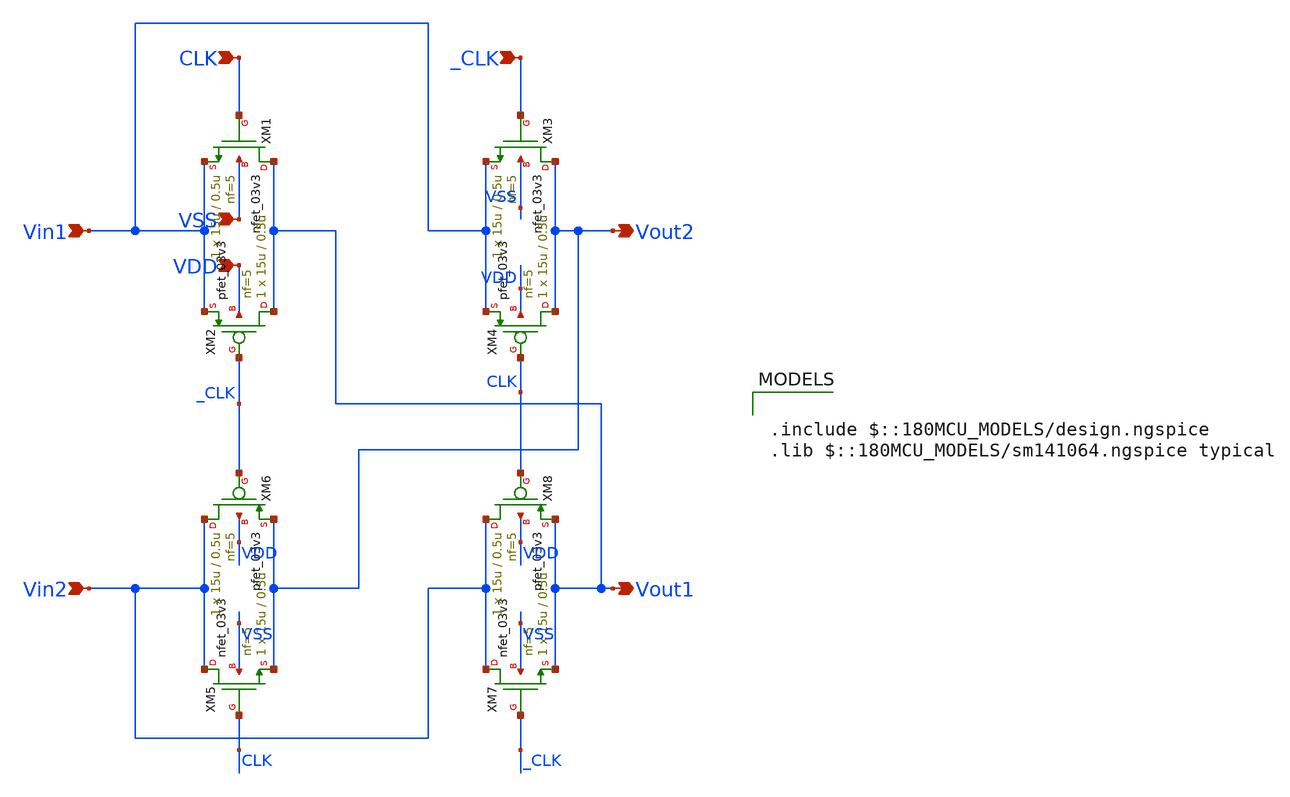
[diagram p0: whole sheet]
** sch_path: ISSCC26/submitted_notebooks/Low Mismatch 4 Channels Instrumentation Amplifier EEG/Chopper Switch/Schmatic and Testbench/switch_A.sch
**.subckt switch_A Vin1 Vout2 Vin2 Vout1 CLK _CLK VDD VSS
*.ipin Vin1
*.opin Vout2
*.ipin Vin2
*.opin Vout1
*.ipin CLK
*.ipin _CLK
*.ipin VDD
*.ipin VSS
XM1 Vout1 CLK Vin1 VSS nfet_03v3 L=0.5u W=15u nf=5 ad='int((nf+1)/2) * W/nf * 0.18u' as='int((nf+2)/2) * W/nf * 0.18u'
+ pd='2*int((nf+1)/2) * (W/nf + 0.18u)' ps='2*int((nf+2)/2) * (W/nf + 0.18u)' nrd='0.18u / W' nrs='0.18u / W'
+ sa=0 sb=0 sd=0 m=1
XM2 Vout1 _CLK Vin1 VDD pfet_03v3 L=0.5u W=15u nf=5 ad='int((nf+1)/2) * W/nf * 0.18u' as='int((nf+2)/2) * W/nf * 0.18u'
+ pd='2*int((nf+1)/2) * (W/nf + 0.18u)' ps='2*int((nf+2)/2) * (W/nf + 0.18u)' nrd='0.18u / W' nrs='0.18u / W'
+ sa=0 sb=0 sd=0 m=1
XM3 Vout2 _CLK Vin1 VSS nfet_03v3 L=0.5u W=15u nf=5 ad='int((nf+1)/2) * W/nf * 0.18u' as='int((nf+2)/2) * W/nf * 0.18u'
+ pd='2*int((nf+1)/2) * (W/nf + 0.18u)' ps='2*int((nf+2)/2) * (W/nf + 0.18u)' nrd='0.18u / W' nrs='0.18u / W'
+ sa=0 sb=0 sd=0 m=1
XM4 Vout2 CLK Vin1 VDD pfet_03v3 L=0.5u W=15u nf=5 ad='int((nf+1)/2) * W/nf * 0.18u' as='int((nf+2)/2) * W/nf * 0.18u'
+ pd='2*int((nf+1)/2) * (W/nf + 0.18u)' ps='2*int((nf+2)/2) * (W/nf + 0.18u)' nrd='0.18u / W' nrs='0.18u / W'
+ sa=0 sb=0 sd=0 m=1
XM5 Vin2 CLK Vout2 VSS nfet_03v3 L=0.5u W=15u nf=5 ad='int((nf+1)/2) * W/nf * 0.18u' as='int((nf+2)/2) * W/nf * 0.18u'
+ pd='2*int((nf+1)/2) * (W/nf + 0.18u)' ps='2*int((nf+2)/2) * (W/nf + 0.18u)' nrd='0.18u / W' nrs='0.18u / W'
+ sa=0 sb=0 sd=0 m=1
XM6 Vin2 _CLK Vout2 VDD pfet_03v3 L=0.5u W=15u nf=5 ad='int((nf+1)/2) * W/nf * 0.18u' as='int((nf+2)/2) * W/nf * 0.18u'
+ pd='2*int((nf+1)/2) * (W/nf + 0.18u)' ps='2*int((nf+2)/2) * (W/nf + 0.18u)' nrd='0.18u / W' nrs='0.18u / W'
+ sa=0 sb=0 sd=0 m=1
XM7 Vin2 _CLK Vout1 VSS nfet_03v3 L=0.5u W=15u nf=5 ad='int((nf+1)/2) * W/nf * 0.18u' as='int((nf+2)/2) * W/nf * 0.18u'
+ pd='2*int((nf+1)/2) * (W/nf + 0.18u)' ps='2*int((nf+2)/2) * (W/nf + 0.18u)' nrd='0.18u / W' nrs='0.18u / W'
+ sa=0 sb=0 sd=0 m=1
XM8 Vin2 CLK Vout1 VDD pfet_03v3 L=0.5u W=15u nf=5 ad='int((nf+1)/2) * W/nf * 0.18u' as='int((nf+2)/2) * W/nf * 0.18u'
+ pd='2*int((nf+1)/2) * (W/nf + 0.18u)' ps='2*int((nf+2)/2) * (W/nf + 0.18u)' nrd='0.18u / W' nrs='0.18u / W'
+ sa=0 sb=0 sd=0 m=1
**** begin user architecture code

.include $::180MCU_MODELS/design.ngspice
.lib $::180MCU_MODELS/sm141064.ngspice typical

**** end user architecture code
**.ends
.end
